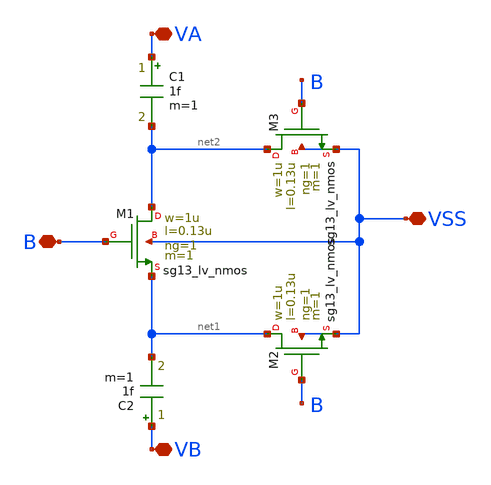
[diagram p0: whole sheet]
** sch_path: analog/core/capb_unit_gen.sch
**.subckt capb_unit_gen VA VSS B VB
*.iopin VA
*.iopin VSS
*.iopin B
*.iopin VB
C1 VA net2 1f m=1
C2 VB net1 1f m=1
XM1 net2 B net1 VSS sg13_lv_nmos w=1u l=0.13u ng=1 m=1 mm_ok=1
XM2 net1 B VSS VSS sg13_lv_nmos w=1u l=0.13u ng=1 m=1 mm_ok=1
XM3 net2 B VSS VSS sg13_lv_nmos w=1u l=0.13u ng=1 m=1 mm_ok=1
**.ends
.end
